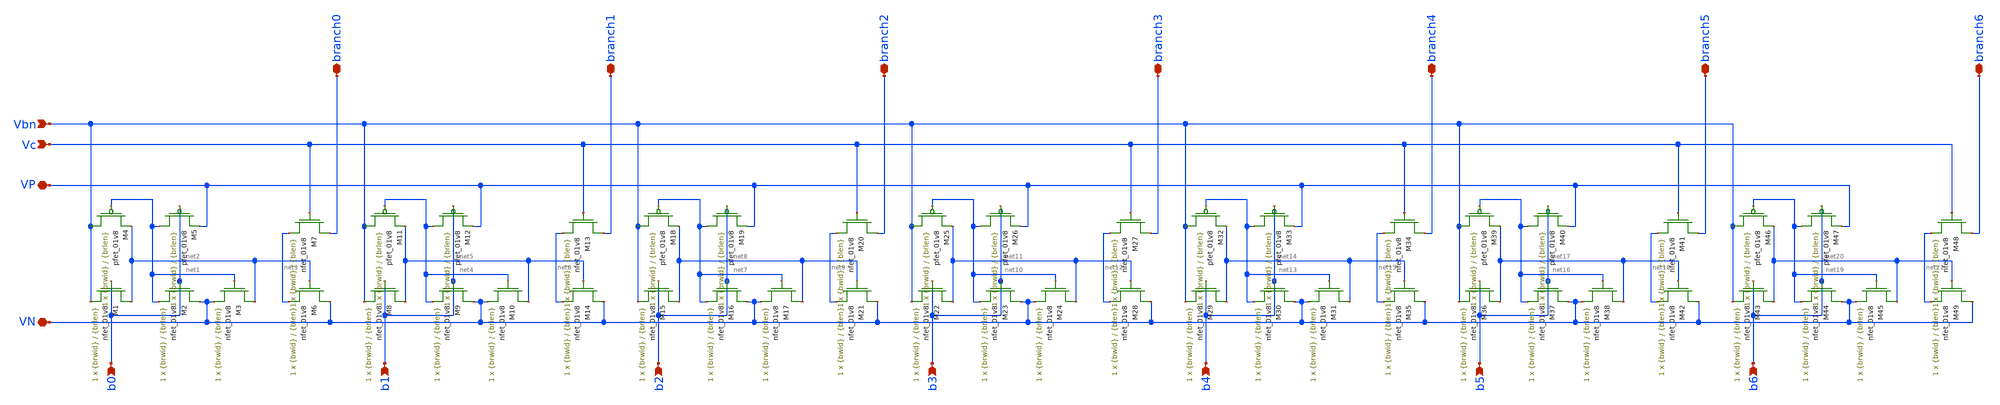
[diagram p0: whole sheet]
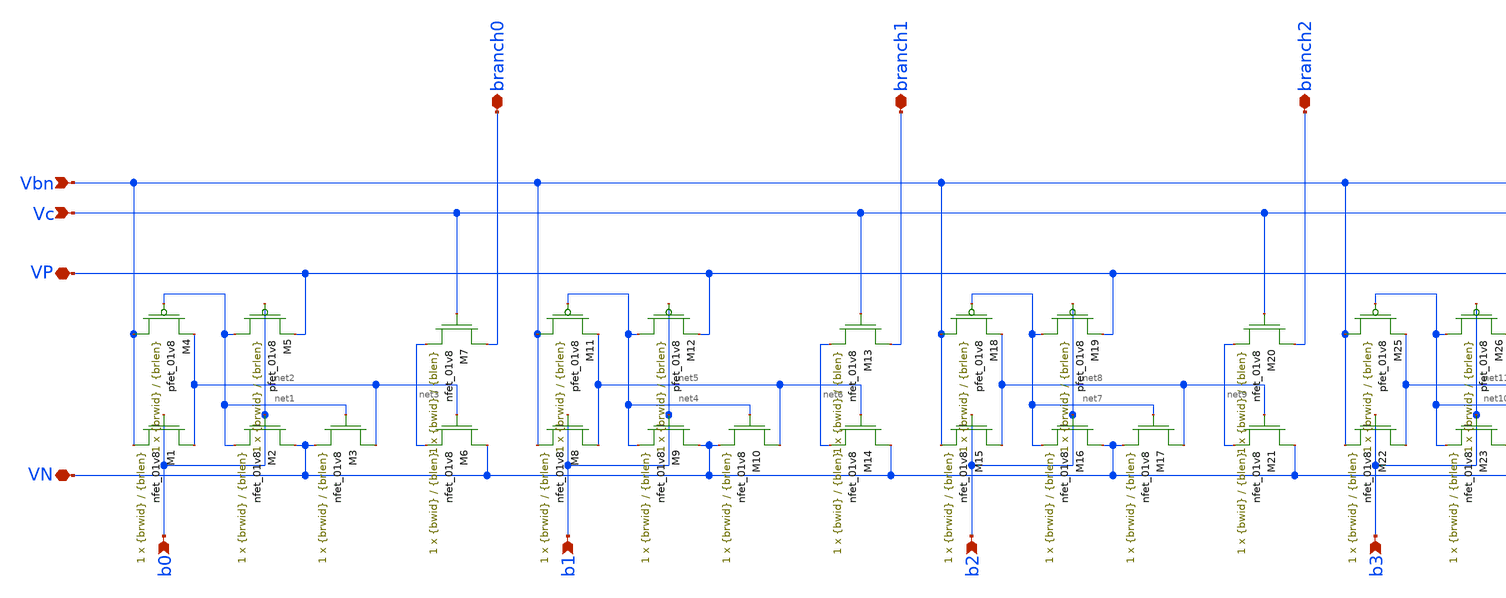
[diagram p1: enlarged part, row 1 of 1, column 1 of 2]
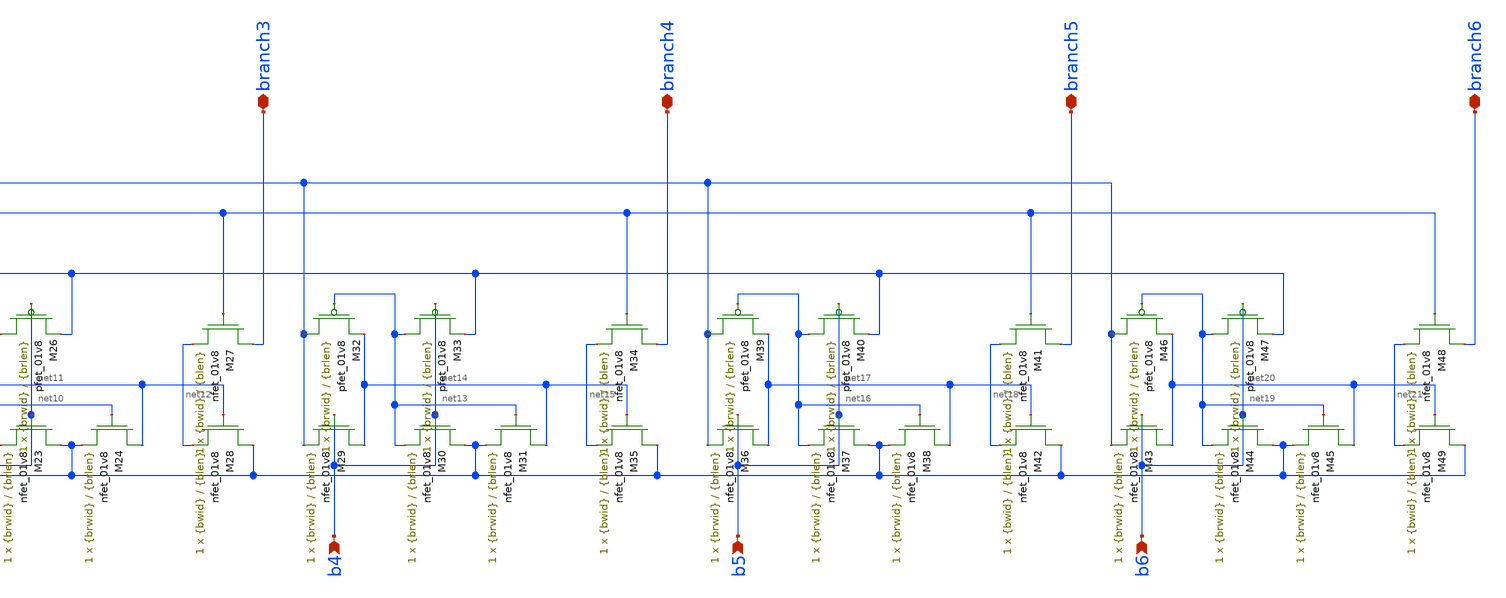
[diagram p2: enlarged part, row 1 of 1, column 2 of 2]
** sch_path: design-files/improved/branchlogic-m2.sch
**.subckt branchlogic-m2 Vc Vbn b0 branch0 b1 branch1 b2 branch2 b3 branch3 b4 branch4 b5 branch5 b6
*+ branch6 VP VN
*.ipin Vc
*.ipin Vbn
*.ipin b0
*.iopin branch0
*.ipin b1
*.iopin branch1
*.ipin b2
*.iopin branch2
*.ipin b3
*.iopin branch3
*.ipin b4
*.iopin branch4
*.ipin b5
*.iopin branch5
*.ipin b6
*.iopin branch6
*.iopin VP
*.iopin VN
XM1 net2 b0 Vbn GND sky130_fd_pr__nfet_01v8 L={brlen} W={brwid} nf=1 ad='int((nf+1)/2) * W/nf * 0.29'
+ as='int((nf+2)/2) * W/nf * 0.29' pd='2*int((nf+1)/2) * (W/nf + 0.29)' ps='2*int((nf+2)/2) * (W/nf + 0.29)'
+ nrd='0.29 / W' nrs='0.29 / W' sa=0 sb=0 sd=0 mult=1 m=1
XM4 Vbn net1 net2 VDD sky130_fd_pr__pfet_01v8 L={brlen} W={brwid} nf=1 ad='int((nf+1)/2) * W/nf * 0.29'
+ as='int((nf+2)/2) * W/nf * 0.29' pd='2*int((nf+1)/2) * (W/nf + 0.29)' ps='2*int((nf+2)/2) * (W/nf + 0.29)'
+ nrd='0.29 / W' nrs='0.29 / W' sa=0 sb=0 sd=0 mult=1 m=1
XM7 branch0 Vc net3 GND sky130_fd_pr__nfet_01v8 L={blen} W={bwid} nf=1 ad='int((nf+1)/2) * W/nf * 0.29'
+ as='int((nf+2)/2) * W/nf * 0.29' pd='2*int((nf+1)/2) * (W/nf + 0.29)' ps='2*int((nf+2)/2) * (W/nf + 0.29)'
+ nrd='0.29 / W' nrs='0.29 / W' sa=0 sb=0 sd=0 mult=1 m=1
XM6 VN net2 net3 GND sky130_fd_pr__nfet_01v8 L={blen} W={bwid} nf=1 ad='int((nf+1)/2) * W/nf * 0.29'
+ as='int((nf+2)/2) * W/nf * 0.29' pd='2*int((nf+1)/2) * (W/nf + 0.29)' ps='2*int((nf+2)/2) * (W/nf + 0.29)'
+ nrd='0.29 / W' nrs='0.29 / W' sa=0 sb=0 sd=0 mult=1 m=1
XM13 branch1 Vc net6 GND sky130_fd_pr__nfet_01v8 L={blen} W={bwid} nf=1 ad='int((nf+1)/2) * W/nf * 0.29'
+ as='int((nf+2)/2) * W/nf * 0.29' pd='2*int((nf+1)/2) * (W/nf + 0.29)' ps='2*int((nf+2)/2) * (W/nf + 0.29)'
+ nrd='0.29 / W' nrs='0.29 / W' sa=0 sb=0 sd=0 mult=1 m=1
XM14 VN net5 net6 GND sky130_fd_pr__nfet_01v8 L={blen} W={bwid} nf=1 ad='int((nf+1)/2) * W/nf * 0.29'
+ as='int((nf+2)/2) * W/nf * 0.29' pd='2*int((nf+1)/2) * (W/nf + 0.29)' ps='2*int((nf+2)/2) * (W/nf + 0.29)'
+ nrd='0.29 / W' nrs='0.29 / W' sa=0 sb=0 sd=0 mult=1 m=1
XM20 branch2 Vc net9 GND sky130_fd_pr__nfet_01v8 L={blen} W={bwid} nf=1 ad='int((nf+1)/2) * W/nf * 0.29'
+ as='int((nf+2)/2) * W/nf * 0.29' pd='2*int((nf+1)/2) * (W/nf + 0.29)' ps='2*int((nf+2)/2) * (W/nf + 0.29)'
+ nrd='0.29 / W' nrs='0.29 / W' sa=0 sb=0 sd=0 mult=1 m=1
XM21 VN net8 net9 GND sky130_fd_pr__nfet_01v8 L={blen} W={bwid} nf=1 ad='int((nf+1)/2) * W/nf * 0.29'
+ as='int((nf+2)/2) * W/nf * 0.29' pd='2*int((nf+1)/2) * (W/nf + 0.29)' ps='2*int((nf+2)/2) * (W/nf + 0.29)'
+ nrd='0.29 / W' nrs='0.29 / W' sa=0 sb=0 sd=0 mult=1 m=1
XM27 branch3 Vc net12 GND sky130_fd_pr__nfet_01v8 L={blen} W={bwid} nf=1 ad='int((nf+1)/2) * W/nf * 0.29'
+ as='int((nf+2)/2) * W/nf * 0.29' pd='2*int((nf+1)/2) * (W/nf + 0.29)' ps='2*int((nf+2)/2) * (W/nf + 0.29)'
+ nrd='0.29 / W' nrs='0.29 / W' sa=0 sb=0 sd=0 mult=1 m=1
XM28 VN net11 net12 GND sky130_fd_pr__nfet_01v8 L={blen} W={bwid} nf=1 ad='int((nf+1)/2) * W/nf * 0.29'
+ as='int((nf+2)/2) * W/nf * 0.29' pd='2*int((nf+1)/2) * (W/nf + 0.29)' ps='2*int((nf+2)/2) * (W/nf + 0.29)'
+ nrd='0.29 / W' nrs='0.29 / W' sa=0 sb=0 sd=0 mult=1 m=1
XM34 branch4 Vc net15 GND sky130_fd_pr__nfet_01v8 L={blen} W={bwid} nf=1 ad='int((nf+1)/2) * W/nf * 0.29'
+ as='int((nf+2)/2) * W/nf * 0.29' pd='2*int((nf+1)/2) * (W/nf + 0.29)' ps='2*int((nf+2)/2) * (W/nf + 0.29)'
+ nrd='0.29 / W' nrs='0.29 / W' sa=0 sb=0 sd=0 mult=1 m=1
XM35 VN net14 net15 GND sky130_fd_pr__nfet_01v8 L={blen} W={bwid} nf=1 ad='int((nf+1)/2) * W/nf * 0.29'
+ as='int((nf+2)/2) * W/nf * 0.29' pd='2*int((nf+1)/2) * (W/nf + 0.29)' ps='2*int((nf+2)/2) * (W/nf + 0.29)'
+ nrd='0.29 / W' nrs='0.29 / W' sa=0 sb=0 sd=0 mult=1 m=1
XM41 branch5 Vc net18 GND sky130_fd_pr__nfet_01v8 L={blen} W={bwid} nf=1 ad='int((nf+1)/2) * W/nf * 0.29'
+ as='int((nf+2)/2) * W/nf * 0.29' pd='2*int((nf+1)/2) * (W/nf + 0.29)' ps='2*int((nf+2)/2) * (W/nf + 0.29)'
+ nrd='0.29 / W' nrs='0.29 / W' sa=0 sb=0 sd=0 mult=1 m=1
XM42 VN net17 net18 GND sky130_fd_pr__nfet_01v8 L={blen} W={bwid} nf=1 ad='int((nf+1)/2) * W/nf * 0.29'
+ as='int((nf+2)/2) * W/nf * 0.29' pd='2*int((nf+1)/2) * (W/nf + 0.29)' ps='2*int((nf+2)/2) * (W/nf + 0.29)'
+ nrd='0.29 / W' nrs='0.29 / W' sa=0 sb=0 sd=0 mult=1 m=1
XM48 branch6 Vc net21 GND sky130_fd_pr__nfet_01v8 L={blen} W={bwid} nf=1 ad='int((nf+1)/2) * W/nf * 0.29'
+ as='int((nf+2)/2) * W/nf * 0.29' pd='2*int((nf+1)/2) * (W/nf + 0.29)' ps='2*int((nf+2)/2) * (W/nf + 0.29)'
+ nrd='0.29 / W' nrs='0.29 / W' sa=0 sb=0 sd=0 mult=1 m=1
XM49 VN net20 net21 GND sky130_fd_pr__nfet_01v8 L={blen} W={bwid} nf=1 ad='int((nf+1)/2) * W/nf * 0.29'
+ as='int((nf+2)/2) * W/nf * 0.29' pd='2*int((nf+1)/2) * (W/nf + 0.29)' ps='2*int((nf+2)/2) * (W/nf + 0.29)'
+ nrd='0.29 / W' nrs='0.29 / W' sa=0 sb=0 sd=0 mult=1 m=1
XM5 net1 b0 VP VDD sky130_fd_pr__pfet_01v8 L={brlen} W={brwid} nf=1 ad='int((nf+1)/2) * W/nf * 0.29'
+ as='int((nf+2)/2) * W/nf * 0.29' pd='2*int((nf+1)/2) * (W/nf + 0.29)' ps='2*int((nf+2)/2) * (W/nf + 0.29)'
+ nrd='0.29 / W' nrs='0.29 / W' sa=0 sb=0 sd=0 mult=1 m=1
XM11 Vbn net4 net5 VDD sky130_fd_pr__pfet_01v8 L={brlen} W={brwid} nf=1 ad='int((nf+1)/2) * W/nf * 0.29'
+ as='int((nf+2)/2) * W/nf * 0.29' pd='2*int((nf+1)/2) * (W/nf + 0.29)' ps='2*int((nf+2)/2) * (W/nf + 0.29)'
+ nrd='0.29 / W' nrs='0.29 / W' sa=0 sb=0 sd=0 mult=1 m=1
XM12 net4 b1 VP VDD sky130_fd_pr__pfet_01v8 L={brlen} W={brwid} nf=1 ad='int((nf+1)/2) * W/nf * 0.29'
+ as='int((nf+2)/2) * W/nf * 0.29' pd='2*int((nf+1)/2) * (W/nf + 0.29)' ps='2*int((nf+2)/2) * (W/nf + 0.29)'
+ nrd='0.29 / W' nrs='0.29 / W' sa=0 sb=0 sd=0 mult=1 m=1
XM18 Vbn net7 net8 VDD sky130_fd_pr__pfet_01v8 L={brlen} W={brwid} nf=1 ad='int((nf+1)/2) * W/nf * 0.29'
+ as='int((nf+2)/2) * W/nf * 0.29' pd='2*int((nf+1)/2) * (W/nf + 0.29)' ps='2*int((nf+2)/2) * (W/nf + 0.29)'
+ nrd='0.29 / W' nrs='0.29 / W' sa=0 sb=0 sd=0 mult=1 m=1
XM19 net7 b2 VP VDD sky130_fd_pr__pfet_01v8 L={brlen} W={brwid} nf=1 ad='int((nf+1)/2) * W/nf * 0.29'
+ as='int((nf+2)/2) * W/nf * 0.29' pd='2*int((nf+1)/2) * (W/nf + 0.29)' ps='2*int((nf+2)/2) * (W/nf + 0.29)'
+ nrd='0.29 / W' nrs='0.29 / W' sa=0 sb=0 sd=0 mult=1 m=1
XM25 Vbn net10 net11 VDD sky130_fd_pr__pfet_01v8 L={brlen} W={brwid} nf=1 ad='int((nf+1)/2) * W/nf * 0.29'
+ as='int((nf+2)/2) * W/nf * 0.29' pd='2*int((nf+1)/2) * (W/nf + 0.29)' ps='2*int((nf+2)/2) * (W/nf + 0.29)'
+ nrd='0.29 / W' nrs='0.29 / W' sa=0 sb=0 sd=0 mult=1 m=1
XM26 net10 b3 VP VDD sky130_fd_pr__pfet_01v8 L={brlen} W={brwid} nf=1 ad='int((nf+1)/2) * W/nf * 0.29'
+ as='int((nf+2)/2) * W/nf * 0.29' pd='2*int((nf+1)/2) * (W/nf + 0.29)' ps='2*int((nf+2)/2) * (W/nf + 0.29)'
+ nrd='0.29 / W' nrs='0.29 / W' sa=0 sb=0 sd=0 mult=1 m=1
XM32 Vbn net13 net14 VDD sky130_fd_pr__pfet_01v8 L={brlen} W={brwid} nf=1 ad='int((nf+1)/2) * W/nf * 0.29'
+ as='int((nf+2)/2) * W/nf * 0.29' pd='2*int((nf+1)/2) * (W/nf + 0.29)' ps='2*int((nf+2)/2) * (W/nf + 0.29)'
+ nrd='0.29 / W' nrs='0.29 / W' sa=0 sb=0 sd=0 mult=1 m=1
XM33 net13 b4 VP VDD sky130_fd_pr__pfet_01v8 L={brlen} W={brwid} nf=1 ad='int((nf+1)/2) * W/nf * 0.29'
+ as='int((nf+2)/2) * W/nf * 0.29' pd='2*int((nf+1)/2) * (W/nf + 0.29)' ps='2*int((nf+2)/2) * (W/nf + 0.29)'
+ nrd='0.29 / W' nrs='0.29 / W' sa=0 sb=0 sd=0 mult=1 m=1
XM39 Vbn net16 net17 VDD sky130_fd_pr__pfet_01v8 L={brlen} W={brwid} nf=1 ad='int((nf+1)/2) * W/nf * 0.29'
+ as='int((nf+2)/2) * W/nf * 0.29' pd='2*int((nf+1)/2) * (W/nf + 0.29)' ps='2*int((nf+2)/2) * (W/nf + 0.29)'
+ nrd='0.29 / W' nrs='0.29 / W' sa=0 sb=0 sd=0 mult=1 m=1
XM40 net16 b5 VP VDD sky130_fd_pr__pfet_01v8 L={brlen} W={brwid} nf=1 ad='int((nf+1)/2) * W/nf * 0.29'
+ as='int((nf+2)/2) * W/nf * 0.29' pd='2*int((nf+1)/2) * (W/nf + 0.29)' ps='2*int((nf+2)/2) * (W/nf + 0.29)'
+ nrd='0.29 / W' nrs='0.29 / W' sa=0 sb=0 sd=0 mult=1 m=1
XM46 Vbn net19 net20 VDD sky130_fd_pr__pfet_01v8 L={brlen} W={brwid} nf=1 ad='int((nf+1)/2) * W/nf * 0.29'
+ as='int((nf+2)/2) * W/nf * 0.29' pd='2*int((nf+1)/2) * (W/nf + 0.29)' ps='2*int((nf+2)/2) * (W/nf + 0.29)'
+ nrd='0.29 / W' nrs='0.29 / W' sa=0 sb=0 sd=0 mult=1 m=1
XM47 net19 b6 VP VDD sky130_fd_pr__pfet_01v8 L={brlen} W={brwid} nf=1 ad='int((nf+1)/2) * W/nf * 0.29'
+ as='int((nf+2)/2) * W/nf * 0.29' pd='2*int((nf+1)/2) * (W/nf + 0.29)' ps='2*int((nf+2)/2) * (W/nf + 0.29)'
+ nrd='0.29 / W' nrs='0.29 / W' sa=0 sb=0 sd=0 mult=1 m=1
XM2 VN b0 net1 GND sky130_fd_pr__nfet_01v8 L={brlen} W={brwid} nf=1 ad='int((nf+1)/2) * W/nf * 0.29'
+ as='int((nf+2)/2) * W/nf * 0.29' pd='2*int((nf+1)/2) * (W/nf + 0.29)' ps='2*int((nf+2)/2) * (W/nf + 0.29)'
+ nrd='0.29 / W' nrs='0.29 / W' sa=0 sb=0 sd=0 mult=1 m=1
XM3 net2 net1 VN GND sky130_fd_pr__nfet_01v8 L={brlen} W={brwid} nf=1 ad='int((nf+1)/2) * W/nf * 0.29'
+ as='int((nf+2)/2) * W/nf * 0.29' pd='2*int((nf+1)/2) * (W/nf + 0.29)' ps='2*int((nf+2)/2) * (W/nf + 0.29)'
+ nrd='0.29 / W' nrs='0.29 / W' sa=0 sb=0 sd=0 mult=1 m=1
XM8 net5 b1 Vbn GND sky130_fd_pr__nfet_01v8 L={brlen} W={brwid} nf=1 ad='int((nf+1)/2) * W/nf * 0.29'
+ as='int((nf+2)/2) * W/nf * 0.29' pd='2*int((nf+1)/2) * (W/nf + 0.29)' ps='2*int((nf+2)/2) * (W/nf + 0.29)'
+ nrd='0.29 / W' nrs='0.29 / W' sa=0 sb=0 sd=0 mult=1 m=1
XM9 VN b1 net4 GND sky130_fd_pr__nfet_01v8 L={brlen} W={brwid} nf=1 ad='int((nf+1)/2) * W/nf * 0.29'
+ as='int((nf+2)/2) * W/nf * 0.29' pd='2*int((nf+1)/2) * (W/nf + 0.29)' ps='2*int((nf+2)/2) * (W/nf + 0.29)'
+ nrd='0.29 / W' nrs='0.29 / W' sa=0 sb=0 sd=0 mult=1 m=1
XM10 net5 net4 VN GND sky130_fd_pr__nfet_01v8 L={brlen} W={brwid} nf=1 ad='int((nf+1)/2) * W/nf * 0.29'
+ as='int((nf+2)/2) * W/nf * 0.29' pd='2*int((nf+1)/2) * (W/nf + 0.29)' ps='2*int((nf+2)/2) * (W/nf + 0.29)'
+ nrd='0.29 / W' nrs='0.29 / W' sa=0 sb=0 sd=0 mult=1 m=1
XM15 net8 b2 Vbn GND sky130_fd_pr__nfet_01v8 L={brlen} W={brwid} nf=1 ad='int((nf+1)/2) * W/nf * 0.29'
+ as='int((nf+2)/2) * W/nf * 0.29' pd='2*int((nf+1)/2) * (W/nf + 0.29)' ps='2*int((nf+2)/2) * (W/nf + 0.29)'
+ nrd='0.29 / W' nrs='0.29 / W' sa=0 sb=0 sd=0 mult=1 m=1
XM16 VN b2 net7 GND sky130_fd_pr__nfet_01v8 L={brlen} W={brwid} nf=1 ad='int((nf+1)/2) * W/nf * 0.29'
+ as='int((nf+2)/2) * W/nf * 0.29' pd='2*int((nf+1)/2) * (W/nf + 0.29)' ps='2*int((nf+2)/2) * (W/nf + 0.29)'
+ nrd='0.29 / W' nrs='0.29 / W' sa=0 sb=0 sd=0 mult=1 m=1
XM17 net8 net7 VN GND sky130_fd_pr__nfet_01v8 L={brlen} W={brwid} nf=1 ad='int((nf+1)/2) * W/nf * 0.29'
+ as='int((nf+2)/2) * W/nf * 0.29' pd='2*int((nf+1)/2) * (W/nf + 0.29)' ps='2*int((nf+2)/2) * (W/nf + 0.29)'
+ nrd='0.29 / W' nrs='0.29 / W' sa=0 sb=0 sd=0 mult=1 m=1
XM22 net11 b3 Vbn GND sky130_fd_pr__nfet_01v8 L={brlen} W={brwid} nf=1 ad='int((nf+1)/2) * W/nf * 0.29'
+ as='int((nf+2)/2) * W/nf * 0.29' pd='2*int((nf+1)/2) * (W/nf + 0.29)' ps='2*int((nf+2)/2) * (W/nf + 0.29)'
+ nrd='0.29 / W' nrs='0.29 / W' sa=0 sb=0 sd=0 mult=1 m=1
XM23 VN b3 net10 GND sky130_fd_pr__nfet_01v8 L={brlen} W={brwid} nf=1 ad='int((nf+1)/2) * W/nf * 0.29'
+ as='int((nf+2)/2) * W/nf * 0.29' pd='2*int((nf+1)/2) * (W/nf + 0.29)' ps='2*int((nf+2)/2) * (W/nf + 0.29)'
+ nrd='0.29 / W' nrs='0.29 / W' sa=0 sb=0 sd=0 mult=1 m=1
XM24 net11 net10 VN GND sky130_fd_pr__nfet_01v8 L={brlen} W={brwid} nf=1 ad='int((nf+1)/2) * W/nf * 0.29'
+ as='int((nf+2)/2) * W/nf * 0.29' pd='2*int((nf+1)/2) * (W/nf + 0.29)' ps='2*int((nf+2)/2) * (W/nf + 0.29)'
+ nrd='0.29 / W' nrs='0.29 / W' sa=0 sb=0 sd=0 mult=1 m=1
XM29 net14 b4 Vbn GND sky130_fd_pr__nfet_01v8 L={brlen} W={brwid} nf=1 ad='int((nf+1)/2) * W/nf * 0.29'
+ as='int((nf+2)/2) * W/nf * 0.29' pd='2*int((nf+1)/2) * (W/nf + 0.29)' ps='2*int((nf+2)/2) * (W/nf + 0.29)'
+ nrd='0.29 / W' nrs='0.29 / W' sa=0 sb=0 sd=0 mult=1 m=1
XM30 VN b4 net13 GND sky130_fd_pr__nfet_01v8 L={brlen} W={brwid} nf=1 ad='int((nf+1)/2) * W/nf * 0.29'
+ as='int((nf+2)/2) * W/nf * 0.29' pd='2*int((nf+1)/2) * (W/nf + 0.29)' ps='2*int((nf+2)/2) * (W/nf + 0.29)'
+ nrd='0.29 / W' nrs='0.29 / W' sa=0 sb=0 sd=0 mult=1 m=1
XM31 net14 net13 VN GND sky130_fd_pr__nfet_01v8 L={brlen} W={brwid} nf=1 ad='int((nf+1)/2) * W/nf * 0.29'
+ as='int((nf+2)/2) * W/nf * 0.29' pd='2*int((nf+1)/2) * (W/nf + 0.29)' ps='2*int((nf+2)/2) * (W/nf + 0.29)'
+ nrd='0.29 / W' nrs='0.29 / W' sa=0 sb=0 sd=0 mult=1 m=1
XM36 net17 b5 Vbn GND sky130_fd_pr__nfet_01v8 L={brlen} W={brwid} nf=1 ad='int((nf+1)/2) * W/nf * 0.29'
+ as='int((nf+2)/2) * W/nf * 0.29' pd='2*int((nf+1)/2) * (W/nf + 0.29)' ps='2*int((nf+2)/2) * (W/nf + 0.29)'
+ nrd='0.29 / W' nrs='0.29 / W' sa=0 sb=0 sd=0 mult=1 m=1
XM37 VN b5 net16 GND sky130_fd_pr__nfet_01v8 L={brlen} W={brwid} nf=1 ad='int((nf+1)/2) * W/nf * 0.29'
+ as='int((nf+2)/2) * W/nf * 0.29' pd='2*int((nf+1)/2) * (W/nf + 0.29)' ps='2*int((nf+2)/2) * (W/nf + 0.29)'
+ nrd='0.29 / W' nrs='0.29 / W' sa=0 sb=0 sd=0 mult=1 m=1
XM38 net17 net16 VN GND sky130_fd_pr__nfet_01v8 L={brlen} W={brwid} nf=1 ad='int((nf+1)/2) * W/nf * 0.29'
+ as='int((nf+2)/2) * W/nf * 0.29' pd='2*int((nf+1)/2) * (W/nf + 0.29)' ps='2*int((nf+2)/2) * (W/nf + 0.29)'
+ nrd='0.29 / W' nrs='0.29 / W' sa=0 sb=0 sd=0 mult=1 m=1
XM43 net20 b6 Vbn GND sky130_fd_pr__nfet_01v8 L={brlen} W={brwid} nf=1 ad='int((nf+1)/2) * W/nf * 0.29'
+ as='int((nf+2)/2) * W/nf * 0.29' pd='2*int((nf+1)/2) * (W/nf + 0.29)' ps='2*int((nf+2)/2) * (W/nf + 0.29)'
+ nrd='0.29 / W' nrs='0.29 / W' sa=0 sb=0 sd=0 mult=1 m=1
XM44 VN b6 net19 GND sky130_fd_pr__nfet_01v8 L={brlen} W={brwid} nf=1 ad='int((nf+1)/2) * W/nf * 0.29'
+ as='int((nf+2)/2) * W/nf * 0.29' pd='2*int((nf+1)/2) * (W/nf + 0.29)' ps='2*int((nf+2)/2) * (W/nf + 0.29)'
+ nrd='0.29 / W' nrs='0.29 / W' sa=0 sb=0 sd=0 mult=1 m=1
XM45 net20 net19 VN GND sky130_fd_pr__nfet_01v8 L={brlen} W={brwid} nf=1 ad='int((nf+1)/2) * W/nf * 0.29'
+ as='int((nf+2)/2) * W/nf * 0.29' pd='2*int((nf+1)/2) * (W/nf + 0.29)' ps='2*int((nf+2)/2) * (W/nf + 0.29)'
+ nrd='0.29 / W' nrs='0.29 / W' sa=0 sb=0 sd=0 mult=1 m=1
**.ends
.end
